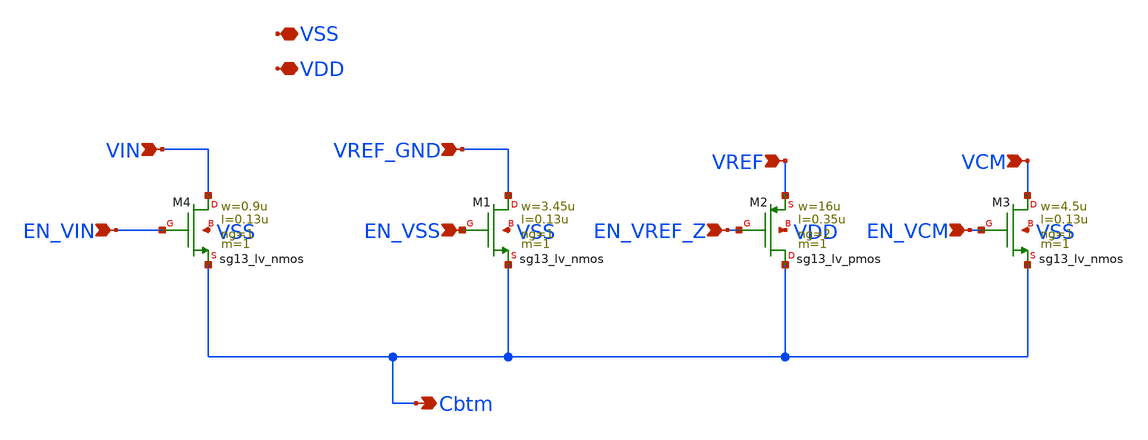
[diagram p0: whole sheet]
** sch_path: schematic/individual_switches/switch_C7.sch
**.subckt switch_C7 VIN EN_VIN VREF_GND EN_VSS Cbtm VSS VREF EN_VREF_Z EN_VCM VCM VDD
*.ipin VIN
*.ipin EN_VIN
*.ipin VREF_GND
*.ipin EN_VSS
*.opin Cbtm
*.iopin VSS
*.ipin VREF
*.ipin EN_VREF_Z
*.ipin EN_VCM
*.ipin VCM
*.iopin VDD
XM4 VIN EN_VIN Cbtm VSS sg13_lv_nmos w=0.9u l=0.13u ng=1 m=1 mm_ok=1
XM1 VREF_GND EN_VSS Cbtm VSS sg13_lv_nmos w=3.45u l=0.13u ng=1 m=1 mm_ok=1
XM2 Cbtm EN_VREF_Z VREF VDD sg13_lv_pmos w=16u l=0.35u ng=2 m=1 mm_ok=1
XM3 VCM EN_VCM Cbtm VSS sg13_lv_nmos w=4.5u l=0.13u ng=1 m=1 mm_ok=1
**.ends
.end
